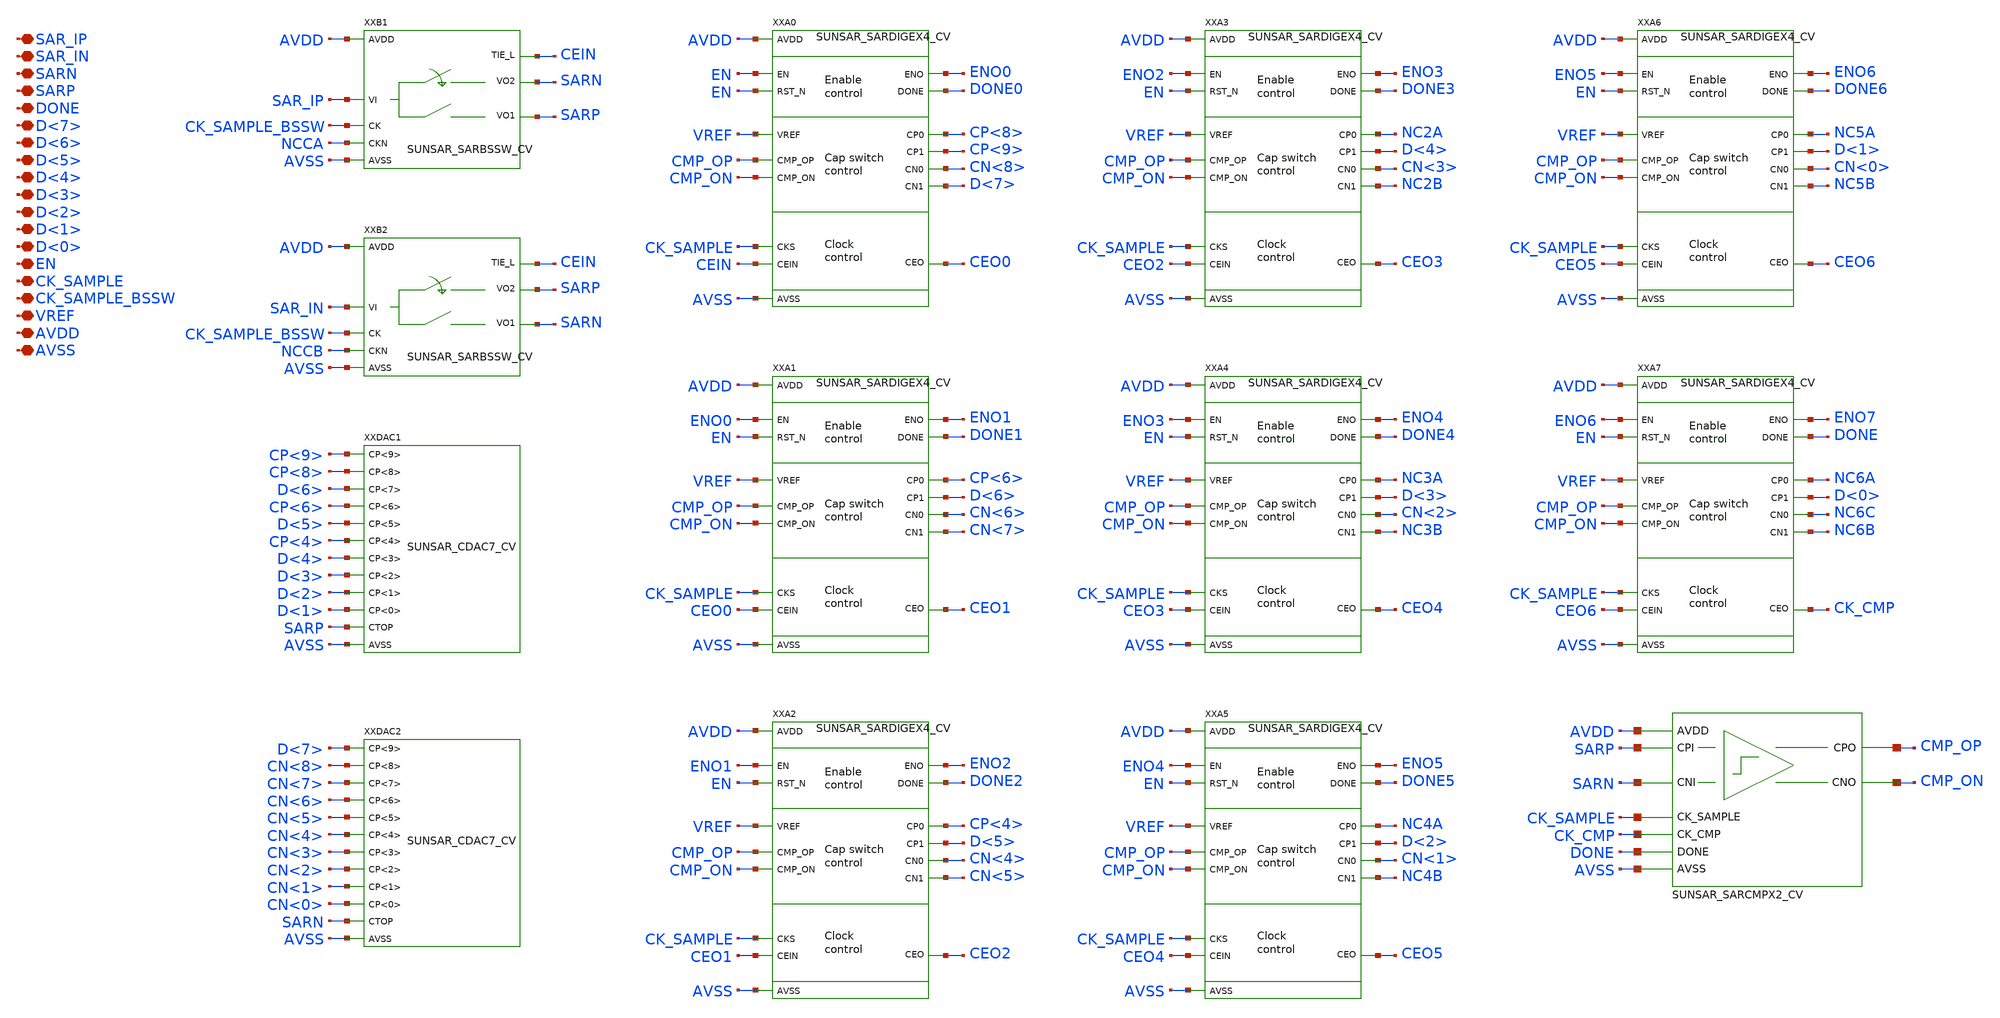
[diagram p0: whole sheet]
** sch_path: design/SUN_SAR9B_SKY130NM/SUNSAR_SAR8B_CV.sch
**.subckt SUNSAR_SAR8B_CV SAR_IP SAR_IN SARN SARP DONE D<7> D<6> D<5> D<4> D<3> D<2> D<1> D<0> EN
*+ CK_SAMPLE CK_SAMPLE_BSSW VREF AVDD AVSS
*.iopin SAR_IP
*.iopin SAR_IN
*.iopin SARN
*.iopin SARP
*.iopin DONE
*.iopin D<7>
*.iopin D<6>
*.iopin D<5>
*.iopin D<4>
*.iopin D<3>
*.iopin D<2>
*.iopin D<1>
*.iopin D<0>
*.iopin EN
*.iopin CK_SAMPLE
*.iopin CK_SAMPLE_BSSW
*.iopin VREF
*.iopin AVDD
*.iopin AVSS
XXB1 SAR_IP CK_SAMPLE_BSSW NCCA CEIN SARP SARN AVDD AVSS SUNSAR_SARBSSW_CV
XXB2 SAR_IN CK_SAMPLE_BSSW NCCB CEIN SARN SARP AVDD AVSS SUNSAR_SARBSSW_CV
XXDAC1 CP<9> CP<8> D<6> CP<6> D<5> CP<4> D<4> D<3> D<2> D<1> SARP AVSS SUNSAR_CDAC7_CV
XXDAC2 D<7> CN<8> CN<7> CN<6> CN<5> CN<4> CN<3> CN<2> CN<1> CN<0> SARN AVSS SUNSAR_CDAC7_CV
XXA0 CMP_OP CMP_ON EN EN ENO0 DONE0 CP<8> CP<9> CN<8> D<7> CEIN CEO0 CK_SAMPLE VREF AVDD AVSS
+ SUNSAR_SARDIGEX4_CV
XXA1 CMP_OP CMP_ON ENO0 EN ENO1 DONE1 CP<6> D<6> CN<6> CN<7> CEO0 CEO1 CK_SAMPLE VREF AVDD AVSS
+ SUNSAR_SARDIGEX4_CV
XXA2 CMP_OP CMP_ON ENO1 EN ENO2 DONE2 CP<4> D<5> CN<4> CN<5> CEO1 CEO2 CK_SAMPLE VREF AVDD AVSS
+ SUNSAR_SARDIGEX4_CV
XXA3 CMP_OP CMP_ON ENO2 EN ENO3 DONE3 NC2A D<4> CN<3> NC2B CEO2 CEO3 CK_SAMPLE VREF AVDD AVSS
+ SUNSAR_SARDIGEX4_CV
XXA4 CMP_OP CMP_ON ENO3 EN ENO4 DONE4 NC3A D<3> CN<2> NC3B CEO3 CEO4 CK_SAMPLE VREF AVDD AVSS
+ SUNSAR_SARDIGEX4_CV
XXA5 CMP_OP CMP_ON ENO4 EN ENO5 DONE5 NC4A D<2> CN<1> NC4B CEO4 CEO5 CK_SAMPLE VREF AVDD AVSS
+ SUNSAR_SARDIGEX4_CV
XXA6 CMP_OP CMP_ON ENO5 EN ENO6 DONE6 NC5A D<1> CN<0> NC5B CEO5 CEO6 CK_SAMPLE VREF AVDD AVSS
+ SUNSAR_SARDIGEX4_CV
XXA7 CMP_OP CMP_ON ENO6 EN ENO7 DONE NC6A D<0> NC6C NC6B CEO6 CK_CMP CK_SAMPLE VREF AVDD AVSS
+ SUNSAR_SARDIGEX4_CV
XXA20 SARP SARN CMP_OP CMP_ON CK_CMP CK_SAMPLE DONE AVDD AVSS SUNSAR_SARCMPX2_CV
**.ends
.end
